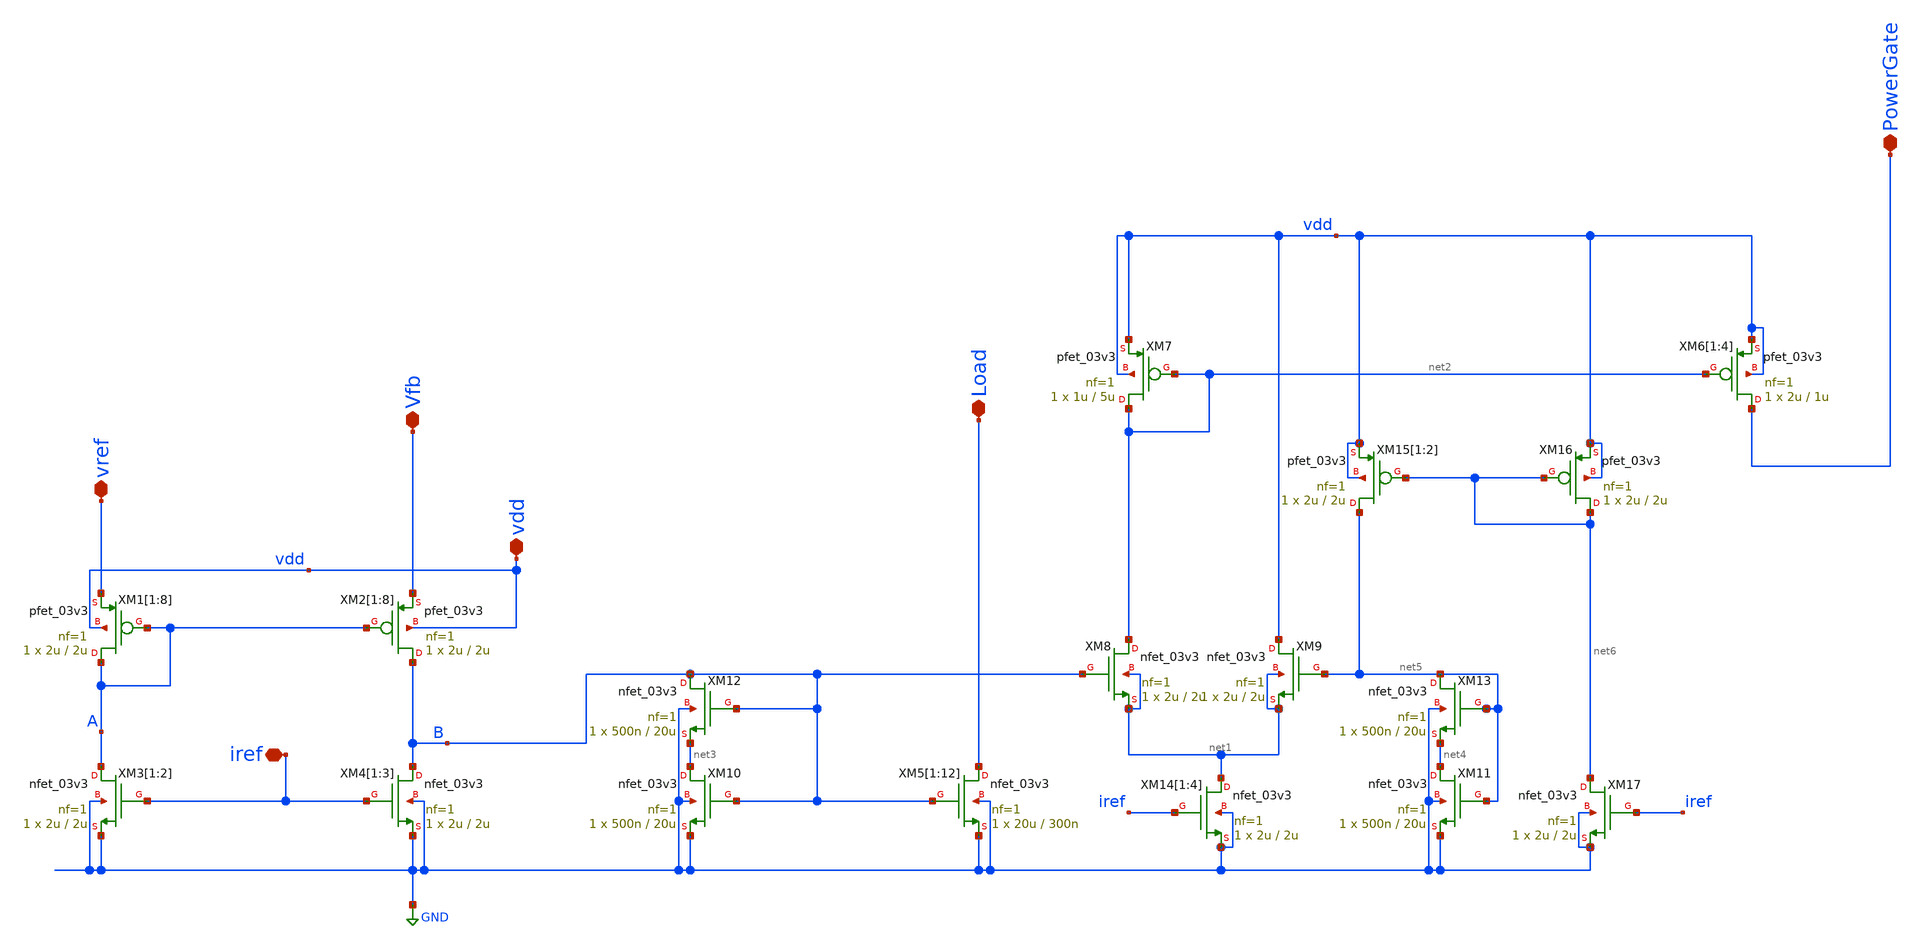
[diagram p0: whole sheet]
** sch_path: Voltage_Reference/LDO/overvoltageProtection.sch
**.subckt overvoltageProtection vref iref vdd Load Vfb PowerGate
*.iopin vref
*.iopin iref
*.iopin vdd
*.iopin Load
*.iopin Vfb
*.iopin PowerGate
XM2[1] B A Vfb vdd pfet_03v3 L=2u W=2u nf=1 ad='int((nf+1)/2) * W/nf * 0.18u' as='int((nf+2)/2) * W/nf * 0.18u'
+ pd='2*int((nf+1)/2) * (W/nf + 0.18u)' ps='2*int((nf+2)/2) * (W/nf + 0.18u)' nrd='0.18u / W' nrs='0.18u / W'
+ sa=0 sb=0 sd=0 m=1
XM2[2] B A Vfb vdd pfet_03v3 L=2u W=2u nf=1 ad='int((nf+1)/2) * W/nf * 0.18u' as='int((nf+2)/2) * W/nf * 0.18u'
+ pd='2*int((nf+1)/2) * (W/nf + 0.18u)' ps='2*int((nf+2)/2) * (W/nf + 0.18u)' nrd='0.18u / W' nrs='0.18u / W'
+ sa=0 sb=0 sd=0 m=1
XM2[3] B A Vfb vdd pfet_03v3 L=2u W=2u nf=1 ad='int((nf+1)/2) * W/nf * 0.18u' as='int((nf+2)/2) * W/nf * 0.18u'
+ pd='2*int((nf+1)/2) * (W/nf + 0.18u)' ps='2*int((nf+2)/2) * (W/nf + 0.18u)' nrd='0.18u / W' nrs='0.18u / W'
+ sa=0 sb=0 sd=0 m=1
XM2[4] B A Vfb vdd pfet_03v3 L=2u W=2u nf=1 ad='int((nf+1)/2) * W/nf * 0.18u' as='int((nf+2)/2) * W/nf * 0.18u'
+ pd='2*int((nf+1)/2) * (W/nf + 0.18u)' ps='2*int((nf+2)/2) * (W/nf + 0.18u)' nrd='0.18u / W' nrs='0.18u / W'
+ sa=0 sb=0 sd=0 m=1
XM2[5] B A Vfb vdd pfet_03v3 L=2u W=2u nf=1 ad='int((nf+1)/2) * W/nf * 0.18u' as='int((nf+2)/2) * W/nf * 0.18u'
+ pd='2*int((nf+1)/2) * (W/nf + 0.18u)' ps='2*int((nf+2)/2) * (W/nf + 0.18u)' nrd='0.18u / W' nrs='0.18u / W'
+ sa=0 sb=0 sd=0 m=1
XM2[6] B A Vfb vdd pfet_03v3 L=2u W=2u nf=1 ad='int((nf+1)/2) * W/nf * 0.18u' as='int((nf+2)/2) * W/nf * 0.18u'
+ pd='2*int((nf+1)/2) * (W/nf + 0.18u)' ps='2*int((nf+2)/2) * (W/nf + 0.18u)' nrd='0.18u / W' nrs='0.18u / W'
+ sa=0 sb=0 sd=0 m=1
XM2[7] B A Vfb vdd pfet_03v3 L=2u W=2u nf=1 ad='int((nf+1)/2) * W/nf * 0.18u' as='int((nf+2)/2) * W/nf * 0.18u'
+ pd='2*int((nf+1)/2) * (W/nf + 0.18u)' ps='2*int((nf+2)/2) * (W/nf + 0.18u)' nrd='0.18u / W' nrs='0.18u / W'
+ sa=0 sb=0 sd=0 m=1
XM2[8] B A Vfb vdd pfet_03v3 L=2u W=2u nf=1 ad='int((nf+1)/2) * W/nf * 0.18u' as='int((nf+2)/2) * W/nf * 0.18u'
+ pd='2*int((nf+1)/2) * (W/nf + 0.18u)' ps='2*int((nf+2)/2) * (W/nf + 0.18u)' nrd='0.18u / W' nrs='0.18u / W'
+ sa=0 sb=0 sd=0 m=1
XM4[1] B iref GND GND nfet_03v3 L=2u W=2u nf=1 ad='int((nf+1)/2) * W/nf * 0.18u' as='int((nf+2)/2) * W/nf * 0.18u'
+ pd='2*int((nf+1)/2) * (W/nf + 0.18u)' ps='2*int((nf+2)/2) * (W/nf + 0.18u)' nrd='0.18u / W' nrs='0.18u / W'
+ sa=0 sb=0 sd=0 m=1
XM4[2] B iref GND GND nfet_03v3 L=2u W=2u nf=1 ad='int((nf+1)/2) * W/nf * 0.18u' as='int((nf+2)/2) * W/nf * 0.18u'
+ pd='2*int((nf+1)/2) * (W/nf + 0.18u)' ps='2*int((nf+2)/2) * (W/nf + 0.18u)' nrd='0.18u / W' nrs='0.18u / W'
+ sa=0 sb=0 sd=0 m=1
XM4[3] B iref GND GND nfet_03v3 L=2u W=2u nf=1 ad='int((nf+1)/2) * W/nf * 0.18u' as='int((nf+2)/2) * W/nf * 0.18u'
+ pd='2*int((nf+1)/2) * (W/nf + 0.18u)' ps='2*int((nf+2)/2) * (W/nf + 0.18u)' nrd='0.18u / W' nrs='0.18u / W'
+ sa=0 sb=0 sd=0 m=1
XM5[1] Load B GND GND nfet_03v3 L=300n W=20u nf=1 ad='int((nf+1)/2) * W/nf * 0.18u' as='int((nf+2)/2) * W/nf * 0.18u'
+ pd='2*int((nf+1)/2) * (W/nf + 0.18u)' ps='2*int((nf+2)/2) * (W/nf + 0.18u)' nrd='0.18u / W' nrs='0.18u / W'
+ sa=0 sb=0 sd=0 m=1
XM5[2] Load B GND GND nfet_03v3 L=300n W=20u nf=1 ad='int((nf+1)/2) * W/nf * 0.18u' as='int((nf+2)/2) * W/nf * 0.18u'
+ pd='2*int((nf+1)/2) * (W/nf + 0.18u)' ps='2*int((nf+2)/2) * (W/nf + 0.18u)' nrd='0.18u / W' nrs='0.18u / W'
+ sa=0 sb=0 sd=0 m=1
XM5[3] Load B GND GND nfet_03v3 L=300n W=20u nf=1 ad='int((nf+1)/2) * W/nf * 0.18u' as='int((nf+2)/2) * W/nf * 0.18u'
+ pd='2*int((nf+1)/2) * (W/nf + 0.18u)' ps='2*int((nf+2)/2) * (W/nf + 0.18u)' nrd='0.18u / W' nrs='0.18u / W'
+ sa=0 sb=0 sd=0 m=1
XM5[4] Load B GND GND nfet_03v3 L=300n W=20u nf=1 ad='int((nf+1)/2) * W/nf * 0.18u' as='int((nf+2)/2) * W/nf * 0.18u'
+ pd='2*int((nf+1)/2) * (W/nf + 0.18u)' ps='2*int((nf+2)/2) * (W/nf + 0.18u)' nrd='0.18u / W' nrs='0.18u / W'
+ sa=0 sb=0 sd=0 m=1
XM5[5] Load B GND GND nfet_03v3 L=300n W=20u nf=1 ad='int((nf+1)/2) * W/nf * 0.18u' as='int((nf+2)/2) * W/nf * 0.18u'
+ pd='2*int((nf+1)/2) * (W/nf + 0.18u)' ps='2*int((nf+2)/2) * (W/nf + 0.18u)' nrd='0.18u / W' nrs='0.18u / W'
+ sa=0 sb=0 sd=0 m=1
XM5[6] Load B GND GND nfet_03v3 L=300n W=20u nf=1 ad='int((nf+1)/2) * W/nf * 0.18u' as='int((nf+2)/2) * W/nf * 0.18u'
+ pd='2*int((nf+1)/2) * (W/nf + 0.18u)' ps='2*int((nf+2)/2) * (W/nf + 0.18u)' nrd='0.18u / W' nrs='0.18u / W'
+ sa=0 sb=0 sd=0 m=1
XM5[7] Load B GND GND nfet_03v3 L=300n W=20u nf=1 ad='int((nf+1)/2) * W/nf * 0.18u' as='int((nf+2)/2) * W/nf * 0.18u'
+ pd='2*int((nf+1)/2) * (W/nf + 0.18u)' ps='2*int((nf+2)/2) * (W/nf + 0.18u)' nrd='0.18u / W' nrs='0.18u / W'
+ sa=0 sb=0 sd=0 m=1
XM5[8] Load B GND GND nfet_03v3 L=300n W=20u nf=1 ad='int((nf+1)/2) * W/nf * 0.18u' as='int((nf+2)/2) * W/nf * 0.18u'
+ pd='2*int((nf+1)/2) * (W/nf + 0.18u)' ps='2*int((nf+2)/2) * (W/nf + 0.18u)' nrd='0.18u / W' nrs='0.18u / W'
+ sa=0 sb=0 sd=0 m=1
XM5[9] Load B GND GND nfet_03v3 L=300n W=20u nf=1 ad='int((nf+1)/2) * W/nf * 0.18u' as='int((nf+2)/2) * W/nf * 0.18u'
+ pd='2*int((nf+1)/2) * (W/nf + 0.18u)' ps='2*int((nf+2)/2) * (W/nf + 0.18u)' nrd='0.18u / W' nrs='0.18u / W'
+ sa=0 sb=0 sd=0 m=1
XM5[10] Load B GND GND nfet_03v3 L=300n W=20u nf=1 ad='int((nf+1)/2) * W/nf * 0.18u' as='int((nf+2)/2) * W/nf * 0.18u'
+ pd='2*int((nf+1)/2) * (W/nf + 0.18u)' ps='2*int((nf+2)/2) * (W/nf + 0.18u)' nrd='0.18u / W' nrs='0.18u / W'
+ sa=0 sb=0 sd=0 m=1
XM5[11] Load B GND GND nfet_03v3 L=300n W=20u nf=1 ad='int((nf+1)/2) * W/nf * 0.18u' as='int((nf+2)/2) * W/nf * 0.18u'
+ pd='2*int((nf+1)/2) * (W/nf + 0.18u)' ps='2*int((nf+2)/2) * (W/nf + 0.18u)' nrd='0.18u / W' nrs='0.18u / W'
+ sa=0 sb=0 sd=0 m=1
XM5[12] Load B GND GND nfet_03v3 L=300n W=20u nf=1 ad='int((nf+1)/2) * W/nf * 0.18u' as='int((nf+2)/2) * W/nf * 0.18u'
+ pd='2*int((nf+1)/2) * (W/nf + 0.18u)' ps='2*int((nf+2)/2) * (W/nf + 0.18u)' nrd='0.18u / W' nrs='0.18u / W'
+ sa=0 sb=0 sd=0 m=1
XM1[1] A A vref vdd pfet_03v3 L=2u W=2u nf=1 ad='int((nf+1)/2) * W/nf * 0.18u' as='int((nf+2)/2) * W/nf * 0.18u'
+ pd='2*int((nf+1)/2) * (W/nf + 0.18u)' ps='2*int((nf+2)/2) * (W/nf + 0.18u)' nrd='0.18u / W' nrs='0.18u / W'
+ sa=0 sb=0 sd=0 m=1
XM1[2] A A vref vdd pfet_03v3 L=2u W=2u nf=1 ad='int((nf+1)/2) * W/nf * 0.18u' as='int((nf+2)/2) * W/nf * 0.18u'
+ pd='2*int((nf+1)/2) * (W/nf + 0.18u)' ps='2*int((nf+2)/2) * (W/nf + 0.18u)' nrd='0.18u / W' nrs='0.18u / W'
+ sa=0 sb=0 sd=0 m=1
XM1[3] A A vref vdd pfet_03v3 L=2u W=2u nf=1 ad='int((nf+1)/2) * W/nf * 0.18u' as='int((nf+2)/2) * W/nf * 0.18u'
+ pd='2*int((nf+1)/2) * (W/nf + 0.18u)' ps='2*int((nf+2)/2) * (W/nf + 0.18u)' nrd='0.18u / W' nrs='0.18u / W'
+ sa=0 sb=0 sd=0 m=1
XM1[4] A A vref vdd pfet_03v3 L=2u W=2u nf=1 ad='int((nf+1)/2) * W/nf * 0.18u' as='int((nf+2)/2) * W/nf * 0.18u'
+ pd='2*int((nf+1)/2) * (W/nf + 0.18u)' ps='2*int((nf+2)/2) * (W/nf + 0.18u)' nrd='0.18u / W' nrs='0.18u / W'
+ sa=0 sb=0 sd=0 m=1
XM1[5] A A vref vdd pfet_03v3 L=2u W=2u nf=1 ad='int((nf+1)/2) * W/nf * 0.18u' as='int((nf+2)/2) * W/nf * 0.18u'
+ pd='2*int((nf+1)/2) * (W/nf + 0.18u)' ps='2*int((nf+2)/2) * (W/nf + 0.18u)' nrd='0.18u / W' nrs='0.18u / W'
+ sa=0 sb=0 sd=0 m=1
XM1[6] A A vref vdd pfet_03v3 L=2u W=2u nf=1 ad='int((nf+1)/2) * W/nf * 0.18u' as='int((nf+2)/2) * W/nf * 0.18u'
+ pd='2*int((nf+1)/2) * (W/nf + 0.18u)' ps='2*int((nf+2)/2) * (W/nf + 0.18u)' nrd='0.18u / W' nrs='0.18u / W'
+ sa=0 sb=0 sd=0 m=1
XM1[7] A A vref vdd pfet_03v3 L=2u W=2u nf=1 ad='int((nf+1)/2) * W/nf * 0.18u' as='int((nf+2)/2) * W/nf * 0.18u'
+ pd='2*int((nf+1)/2) * (W/nf + 0.18u)' ps='2*int((nf+2)/2) * (W/nf + 0.18u)' nrd='0.18u / W' nrs='0.18u / W'
+ sa=0 sb=0 sd=0 m=1
XM1[8] A A vref vdd pfet_03v3 L=2u W=2u nf=1 ad='int((nf+1)/2) * W/nf * 0.18u' as='int((nf+2)/2) * W/nf * 0.18u'
+ pd='2*int((nf+1)/2) * (W/nf + 0.18u)' ps='2*int((nf+2)/2) * (W/nf + 0.18u)' nrd='0.18u / W' nrs='0.18u / W'
+ sa=0 sb=0 sd=0 m=1
XM3[1] A iref GND GND nfet_03v3 L=2u W=2u nf=1 ad='int((nf+1)/2) * W/nf * 0.18u' as='int((nf+2)/2) * W/nf * 0.18u'
+ pd='2*int((nf+1)/2) * (W/nf + 0.18u)' ps='2*int((nf+2)/2) * (W/nf + 0.18u)' nrd='0.18u / W' nrs='0.18u / W'
+ sa=0 sb=0 sd=0 m=1
XM3[2] A iref GND GND nfet_03v3 L=2u W=2u nf=1 ad='int((nf+1)/2) * W/nf * 0.18u' as='int((nf+2)/2) * W/nf * 0.18u'
+ pd='2*int((nf+1)/2) * (W/nf + 0.18u)' ps='2*int((nf+2)/2) * (W/nf + 0.18u)' nrd='0.18u / W' nrs='0.18u / W'
+ sa=0 sb=0 sd=0 m=1
XM6[1] PowerGate net2 vdd vdd pfet_03v3 L=1u W=2u nf=1 ad='int((nf+1)/2) * W/nf * 0.18u' as='int((nf+2)/2) * W/nf * 0.18u'
+ pd='2*int((nf+1)/2) * (W/nf + 0.18u)' ps='2*int((nf+2)/2) * (W/nf + 0.18u)' nrd='0.18u / W' nrs='0.18u / W'
+ sa=0 sb=0 sd=0 m=1
XM6[2] PowerGate net2 vdd vdd pfet_03v3 L=1u W=2u nf=1 ad='int((nf+1)/2) * W/nf * 0.18u' as='int((nf+2)/2) * W/nf * 0.18u'
+ pd='2*int((nf+1)/2) * (W/nf + 0.18u)' ps='2*int((nf+2)/2) * (W/nf + 0.18u)' nrd='0.18u / W' nrs='0.18u / W'
+ sa=0 sb=0 sd=0 m=1
XM6[3] PowerGate net2 vdd vdd pfet_03v3 L=1u W=2u nf=1 ad='int((nf+1)/2) * W/nf * 0.18u' as='int((nf+2)/2) * W/nf * 0.18u'
+ pd='2*int((nf+1)/2) * (W/nf + 0.18u)' ps='2*int((nf+2)/2) * (W/nf + 0.18u)' nrd='0.18u / W' nrs='0.18u / W'
+ sa=0 sb=0 sd=0 m=1
XM6[4] PowerGate net2 vdd vdd pfet_03v3 L=1u W=2u nf=1 ad='int((nf+1)/2) * W/nf * 0.18u' as='int((nf+2)/2) * W/nf * 0.18u'
+ pd='2*int((nf+1)/2) * (W/nf + 0.18u)' ps='2*int((nf+2)/2) * (W/nf + 0.18u)' nrd='0.18u / W' nrs='0.18u / W'
+ sa=0 sb=0 sd=0 m=1
XM7 net2 net2 vdd vdd pfet_03v3 L=5u W=1u nf=1 ad='int((nf+1)/2) * W/nf * 0.18u' as='int((nf+2)/2) * W/nf * 0.18u'
+ pd='2*int((nf+1)/2) * (W/nf + 0.18u)' ps='2*int((nf+2)/2) * (W/nf + 0.18u)' nrd='0.18u / W' nrs='0.18u / W'
+ sa=0 sb=0 sd=0 m=1
XM8 net2 B net1 net1 nfet_03v3 L=2u W=2u nf=1 ad='int((nf+1)/2) * W/nf * 0.18u' as='int((nf+2)/2) * W/nf * 0.18u'
+ pd='2*int((nf+1)/2) * (W/nf + 0.18u)' ps='2*int((nf+2)/2) * (W/nf + 0.18u)' nrd='0.18u / W' nrs='0.18u / W'
+ sa=0 sb=0 sd=0 m=1
XM10 net3 B GND GND nfet_03v3 L=20u W=500n nf=1 ad='int((nf+1)/2) * W/nf * 0.18u' as='int((nf+2)/2) * W/nf * 0.18u'
+ pd='2*int((nf+1)/2) * (W/nf + 0.18u)' ps='2*int((nf+2)/2) * (W/nf + 0.18u)' nrd='0.18u / W' nrs='0.18u / W'
+ sa=0 sb=0 sd=0 m=1
XM12 B B net3 GND nfet_03v3 L=20u W=500n nf=1 ad='int((nf+1)/2) * W/nf * 0.18u' as='int((nf+2)/2) * W/nf * 0.18u'
+ pd='2*int((nf+1)/2) * (W/nf + 0.18u)' ps='2*int((nf+2)/2) * (W/nf + 0.18u)' nrd='0.18u / W' nrs='0.18u / W'
+ sa=0 sb=0 sd=0 m=1
XM9 vdd net5 net1 net1 nfet_03v3 L=2u W=2u nf=1 ad='int((nf+1)/2) * W/nf * 0.18u' as='int((nf+2)/2) * W/nf * 0.18u'
+ pd='2*int((nf+1)/2) * (W/nf + 0.18u)' ps='2*int((nf+2)/2) * (W/nf + 0.18u)' nrd='0.18u / W' nrs='0.18u / W'
+ sa=0 sb=0 sd=0 m=1
XM11 net4 net5 GND GND nfet_03v3 L=20u W=500n nf=1 ad='int((nf+1)/2) * W/nf * 0.18u' as='int((nf+2)/2) * W/nf * 0.18u'
+ pd='2*int((nf+1)/2) * (W/nf + 0.18u)' ps='2*int((nf+2)/2) * (W/nf + 0.18u)' nrd='0.18u / W' nrs='0.18u / W'
+ sa=0 sb=0 sd=0 m=1
XM13 net5 net5 net4 GND nfet_03v3 L=20u W=500n nf=1 ad='int((nf+1)/2) * W/nf * 0.18u' as='int((nf+2)/2) * W/nf * 0.18u'
+ pd='2*int((nf+1)/2) * (W/nf + 0.18u)' ps='2*int((nf+2)/2) * (W/nf + 0.18u)' nrd='0.18u / W' nrs='0.18u / W'
+ sa=0 sb=0 sd=0 m=1
XM14[1] net1 iref GND GND nfet_03v3 L=2u W=2u nf=1 ad='int((nf+1)/2) * W/nf * 0.18u' as='int((nf+2)/2) * W/nf * 0.18u'
+ pd='2*int((nf+1)/2) * (W/nf + 0.18u)' ps='2*int((nf+2)/2) * (W/nf + 0.18u)' nrd='0.18u / W' nrs='0.18u / W'
+ sa=0 sb=0 sd=0 m=1
XM14[2] net1 iref GND GND nfet_03v3 L=2u W=2u nf=1 ad='int((nf+1)/2) * W/nf * 0.18u' as='int((nf+2)/2) * W/nf * 0.18u'
+ pd='2*int((nf+1)/2) * (W/nf + 0.18u)' ps='2*int((nf+2)/2) * (W/nf + 0.18u)' nrd='0.18u / W' nrs='0.18u / W'
+ sa=0 sb=0 sd=0 m=1
XM14[3] net1 iref GND GND nfet_03v3 L=2u W=2u nf=1 ad='int((nf+1)/2) * W/nf * 0.18u' as='int((nf+2)/2) * W/nf * 0.18u'
+ pd='2*int((nf+1)/2) * (W/nf + 0.18u)' ps='2*int((nf+2)/2) * (W/nf + 0.18u)' nrd='0.18u / W' nrs='0.18u / W'
+ sa=0 sb=0 sd=0 m=1
XM14[4] net1 iref GND GND nfet_03v3 L=2u W=2u nf=1 ad='int((nf+1)/2) * W/nf * 0.18u' as='int((nf+2)/2) * W/nf * 0.18u'
+ pd='2*int((nf+1)/2) * (W/nf + 0.18u)' ps='2*int((nf+2)/2) * (W/nf + 0.18u)' nrd='0.18u / W' nrs='0.18u / W'
+ sa=0 sb=0 sd=0 m=1
XM15[1] net5 net6 vdd vdd pfet_03v3 L=2u W=2u nf=1 ad='int((nf+1)/2) * W/nf * 0.18u' as='int((nf+2)/2) * W/nf * 0.18u'
+ pd='2*int((nf+1)/2) * (W/nf + 0.18u)' ps='2*int((nf+2)/2) * (W/nf + 0.18u)' nrd='0.18u / W' nrs='0.18u / W'
+ sa=0 sb=0 sd=0 m=1
XM15[2] net5 net6 vdd vdd pfet_03v3 L=2u W=2u nf=1 ad='int((nf+1)/2) * W/nf * 0.18u' as='int((nf+2)/2) * W/nf * 0.18u'
+ pd='2*int((nf+1)/2) * (W/nf + 0.18u)' ps='2*int((nf+2)/2) * (W/nf + 0.18u)' nrd='0.18u / W' nrs='0.18u / W'
+ sa=0 sb=0 sd=0 m=1
XM16 net6 net6 vdd vdd pfet_03v3 L=2u W=2u nf=1 ad='int((nf+1)/2) * W/nf * 0.18u' as='int((nf+2)/2) * W/nf * 0.18u'
+ pd='2*int((nf+1)/2) * (W/nf + 0.18u)' ps='2*int((nf+2)/2) * (W/nf + 0.18u)' nrd='0.18u / W' nrs='0.18u / W'
+ sa=0 sb=0 sd=0 m=1
XM17 net6 iref GND GND nfet_03v3 L=2u W=2u nf=1 ad='int((nf+1)/2) * W/nf * 0.18u' as='int((nf+2)/2) * W/nf * 0.18u'
+ pd='2*int((nf+1)/2) * (W/nf + 0.18u)' ps='2*int((nf+2)/2) * (W/nf + 0.18u)' nrd='0.18u / W' nrs='0.18u / W'
+ sa=0 sb=0 sd=0 m=1
**.ends
.GLOBAL GND
.end
